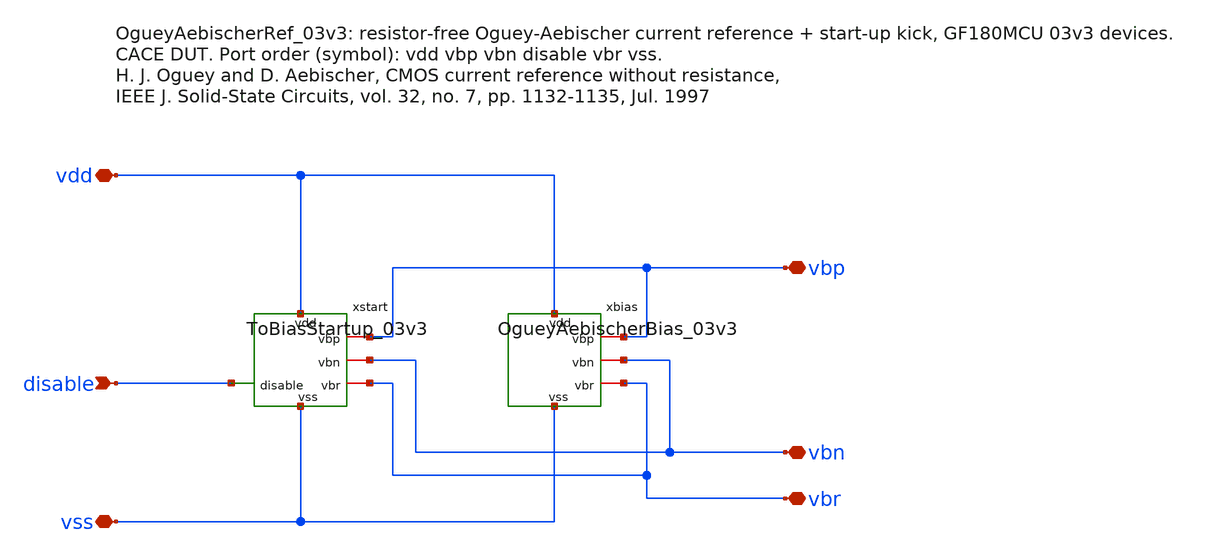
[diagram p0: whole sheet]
** sch_path: macros/OgueyAebischerBias/schematic/xschem/OgueyAebischerRef_03v3.sch
**.subckt OgueyAebischerRef_03v3 vdd vbp vbn disable vbr vss
*.iopin vdd
*.iopin vbp
*.iopin vbn
*.ipin disable
*.iopin vbr
*.iopin vss
xbias vdd vbp vbn vbr vss OgueyAebischerBias_03v3
xstart vdd vbp vbn disable vbr vss ToBiasStartup_03v3
**.ends
.end
